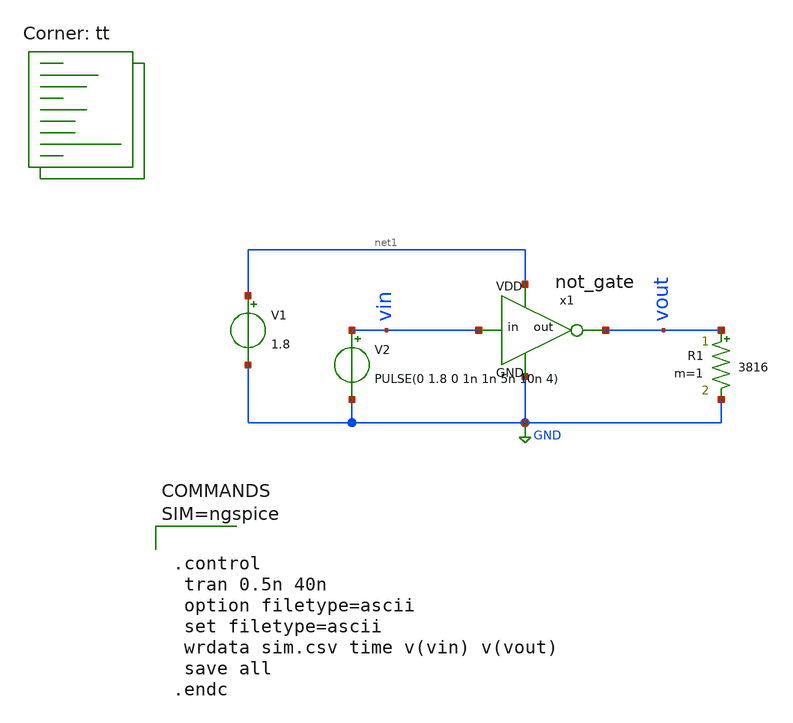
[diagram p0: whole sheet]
** sch_path: tp6/simulation/sim.sch
**.subckt sim
V1 net1 GND 1.8
V2 vin GND PULSE(0 1.8 0 1n 1n 5n 10n 4)
R1 vout GND 3816 m=1
x1 vout vin GND net1 not_gate
**** begin user architecture code
.lib $::SKYWATER_MODELS/sky130.lib.spice tt



.control
 tran 0.5n 40n
 option filetype=ascii
 set filetype=ascii
 wrdata sim.csv time v(vin) v(vout)
 save all
.endc



**** end user architecture code
**.ends
.GLOBAL GND
.end
